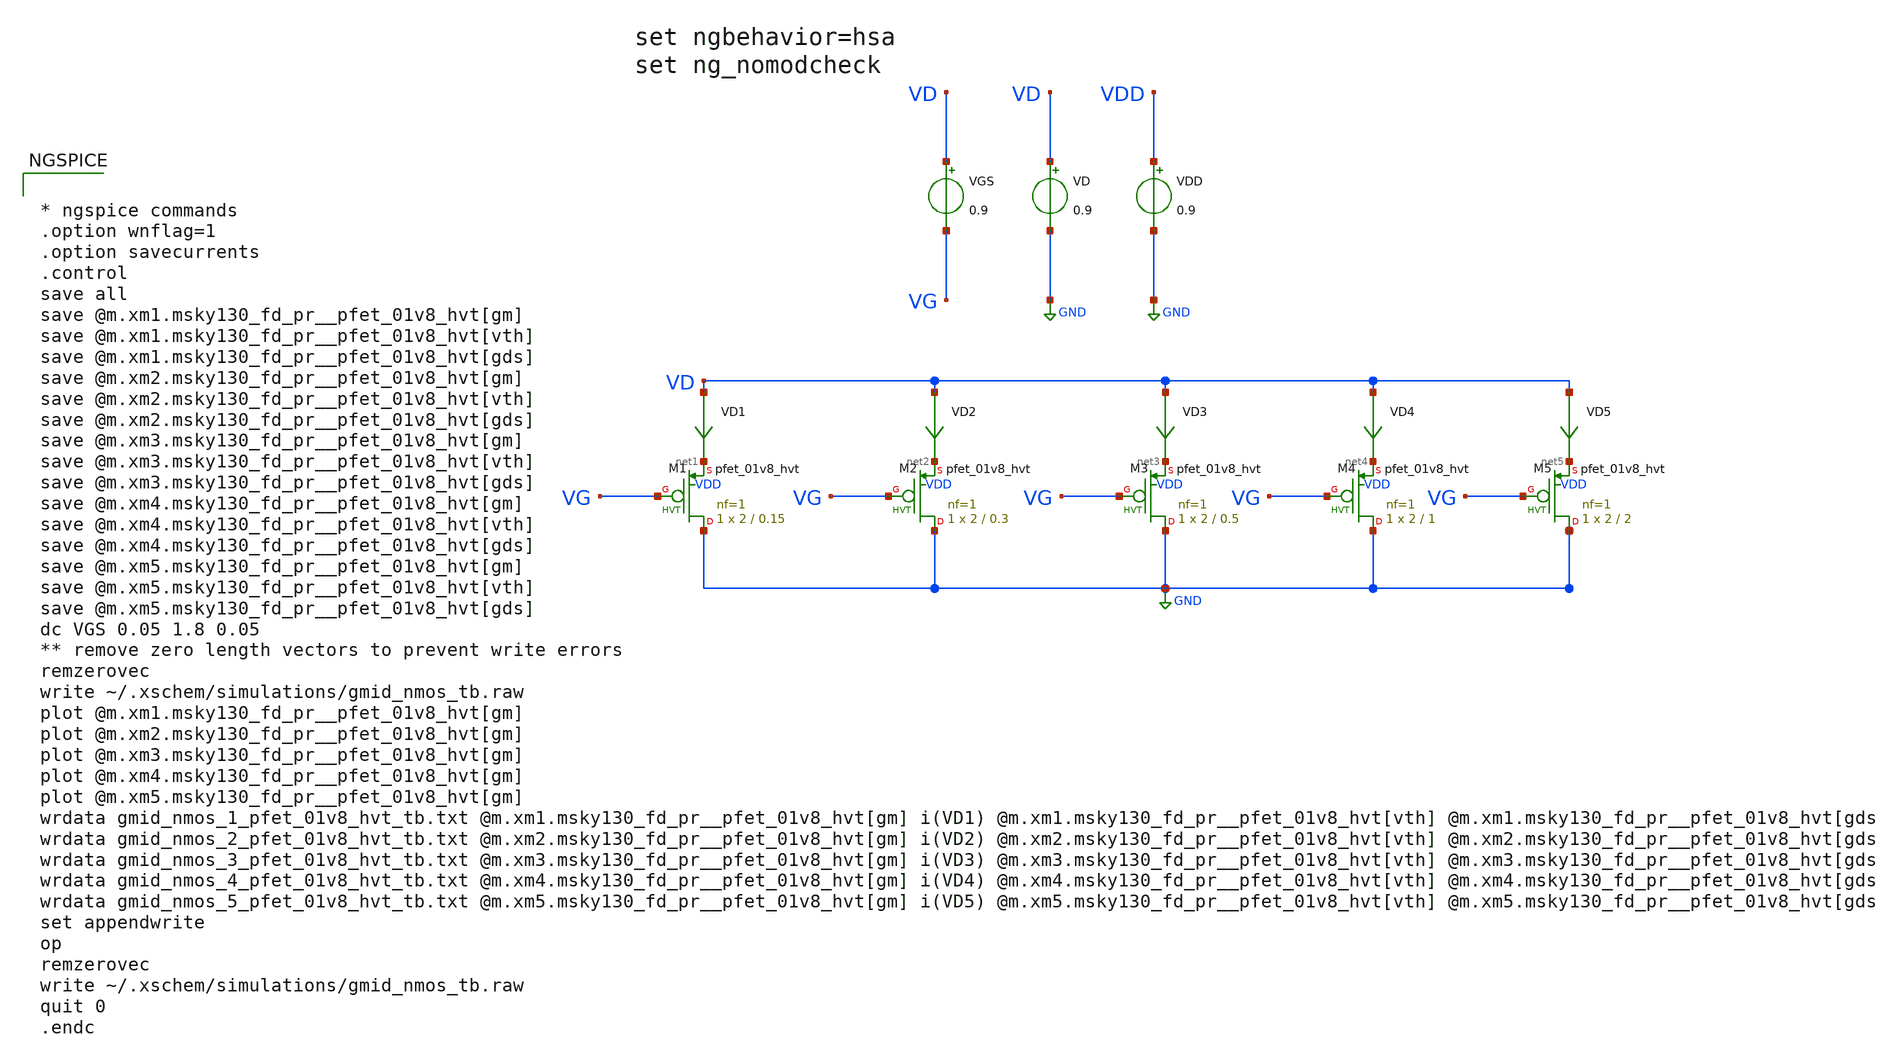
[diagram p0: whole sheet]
** sch_path: designs/gmid_pmos_1v8_hvt_tb.sch
**.subckt gmid_pmos_1v8_hvt_tb
VGS VD VG 0.9
VD VD GND 0.9
VD1 VD net1 0
.save i(vd1)
VD2 VD net2 0
.save i(vd2)
XM1 GND VG net1 VDD sky130_fd_pr__pfet_01v8_hvt L=0.15 W=2 nf=1 ad='int((nf+1)/2) * W/nf * 0.29' as='int((nf+2)/2) * W/nf * 0.29'
+ pd='2*int((nf+1)/2) * (W/nf + 0.29)' ps='2*int((nf+2)/2) * (W/nf + 0.29)' nrd='0.29 / W' nrs='0.29 / W'
+ sa=0 sb=0 sd=0 mult=1 m=1
XM2 GND VG net2 VDD sky130_fd_pr__pfet_01v8_hvt L=0.3 W=2 nf=1 ad='int((nf+1)/2) * W/nf * 0.29' as='int((nf+2)/2) * W/nf * 0.29'
+ pd='2*int((nf+1)/2) * (W/nf + 0.29)' ps='2*int((nf+2)/2) * (W/nf + 0.29)' nrd='0.29 / W' nrs='0.29 / W'
+ sa=0 sb=0 sd=0 mult=1 m=1
VD3 VD net3 0
.save i(vd3)
XM3 GND VG net3 VDD sky130_fd_pr__pfet_01v8_hvt L=0.5 W=2 nf=1 ad='int((nf+1)/2) * W/nf * 0.29' as='int((nf+2)/2) * W/nf * 0.29'
+ pd='2*int((nf+1)/2) * (W/nf + 0.29)' ps='2*int((nf+2)/2) * (W/nf + 0.29)' nrd='0.29 / W' nrs='0.29 / W'
+ sa=0 sb=0 sd=0 mult=1 m=1
VD4 VD net4 0
.save i(vd4)
XM4 GND VG net4 VDD sky130_fd_pr__pfet_01v8_hvt L=1 W=2 nf=1 ad='int((nf+1)/2) * W/nf * 0.29' as='int((nf+2)/2) * W/nf * 0.29'
+ pd='2*int((nf+1)/2) * (W/nf + 0.29)' ps='2*int((nf+2)/2) * (W/nf + 0.29)' nrd='0.29 / W' nrs='0.29 / W'
+ sa=0 sb=0 sd=0 mult=1 m=1
VD5 VD net5 0
.save i(vd5)
XM5 GND VG net5 VDD sky130_fd_pr__pfet_01v8_hvt L=2 W=2 nf=1 ad='int((nf+1)/2) * W/nf * 0.29' as='int((nf+2)/2) * W/nf * 0.29'
+ pd='2*int((nf+1)/2) * (W/nf + 0.29)' ps='2*int((nf+2)/2) * (W/nf + 0.29)' nrd='0.29 / W' nrs='0.29 / W'
+ sa=0 sb=0 sd=0 mult=1 m=1
VDD VDD GND 0.9
**** begin user architecture code

** opencircuitdesign pdks install
.lib $::SKYWATER_MODELS/sky130.lib.spice ff




* ngspice commands
.option wnflag=1
.option savecurrents
.control
save all
save @m.xm1.msky130_fd_pr__pfet_01v8_hvt[gm]
save @m.xm1.msky130_fd_pr__pfet_01v8_hvt[vth]
save @m.xm1.msky130_fd_pr__pfet_01v8_hvt[gds]
save @m.xm2.msky130_fd_pr__pfet_01v8_hvt[gm]
save @m.xm2.msky130_fd_pr__pfet_01v8_hvt[vth]
save @m.xm2.msky130_fd_pr__pfet_01v8_hvt[gds]
save @m.xm3.msky130_fd_pr__pfet_01v8_hvt[gm]
save @m.xm3.msky130_fd_pr__pfet_01v8_hvt[vth]
save @m.xm3.msky130_fd_pr__pfet_01v8_hvt[gds]
save @m.xm4.msky130_fd_pr__pfet_01v8_hvt[gm]
save @m.xm4.msky130_fd_pr__pfet_01v8_hvt[vth]
save @m.xm4.msky130_fd_pr__pfet_01v8_hvt[gds]
save @m.xm5.msky130_fd_pr__pfet_01v8_hvt[gm]
save @m.xm5.msky130_fd_pr__pfet_01v8_hvt[vth]
save @m.xm5.msky130_fd_pr__pfet_01v8_hvt[gds]
dc VGS 0.05 1.8 0.05
** remove zero length vectors to prevent write errors
remzerovec
write ~/.xschem/simulations/gmid_nmos_tb.raw
plot @m.xm1.msky130_fd_pr__pfet_01v8_hvt[gm]
plot @m.xm2.msky130_fd_pr__pfet_01v8_hvt[gm]
plot @m.xm3.msky130_fd_pr__pfet_01v8_hvt[gm]
plot @m.xm4.msky130_fd_pr__pfet_01v8_hvt[gm]
plot @m.xm5.msky130_fd_pr__pfet_01v8_hvt[gm]
wrdata gmid_nmos_1_pfet_01v8_hvt_tb.txt @m.xm1.msky130_fd_pr__pfet_01v8_hvt[gm] i(VD1)
+ @m.xm1.msky130_fd_pr__pfet_01v8_hvt[vth] @m.xm1.msky130_fd_pr__pfet_01v8_hvt[gds]
wrdata gmid_nmos_2_pfet_01v8_hvt_tb.txt @m.xm2.msky130_fd_pr__pfet_01v8_hvt[gm] i(VD2)
+ @m.xm2.msky130_fd_pr__pfet_01v8_hvt[vth] @m.xm2.msky130_fd_pr__pfet_01v8_hvt[gds]
wrdata gmid_nmos_3_pfet_01v8_hvt_tb.txt @m.xm3.msky130_fd_pr__pfet_01v8_hvt[gm] i(VD3)
+ @m.xm3.msky130_fd_pr__pfet_01v8_hvt[vth] @m.xm3.msky130_fd_pr__pfet_01v8_hvt[gds]
wrdata gmid_nmos_4_pfet_01v8_hvt_tb.txt @m.xm4.msky130_fd_pr__pfet_01v8_hvt[gm] i(VD4)
+ @m.xm4.msky130_fd_pr__pfet_01v8_hvt[vth] @m.xm4.msky130_fd_pr__pfet_01v8_hvt[gds]
wrdata gmid_nmos_5_pfet_01v8_hvt_tb.txt @m.xm5.msky130_fd_pr__pfet_01v8_hvt[gm] i(VD5)
+ @m.xm5.msky130_fd_pr__pfet_01v8_hvt[vth] @m.xm5.msky130_fd_pr__pfet_01v8_hvt[gds]
set appendwrite
op
remzerovec
write ~/.xschem/simulations/gmid_nmos_tb.raw
quit 0
.endc


**** end user architecture code
**.ends
.GLOBAL GND
.end
